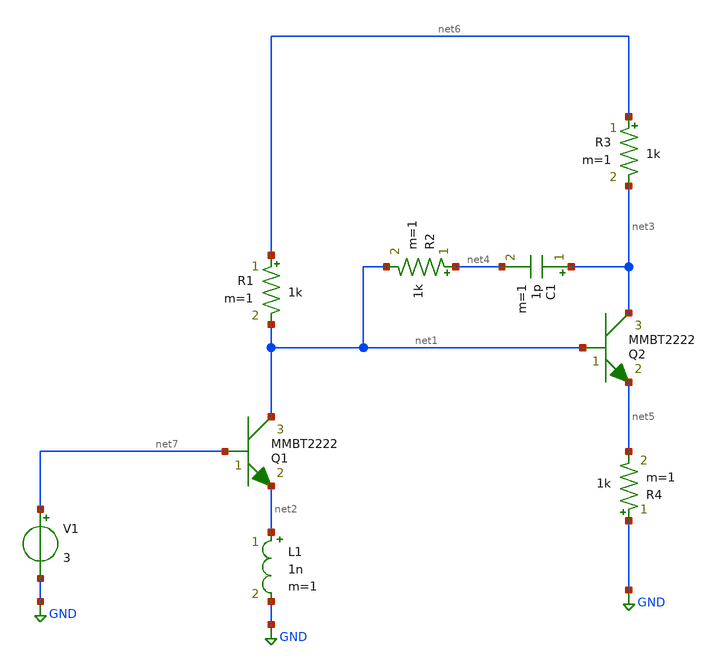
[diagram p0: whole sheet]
** sch_path: poweramp/poweramp.sch
**.subckt poweramp
Q2 net3 net1 net5 MMBT2222 area=1 m=1
Q1 net1 net7 net2 MMBT2222 area=1 m=1
R1 net6 net1 1k m=1
R2 net4 net1 1k m=1
C1 net3 net4 1p m=1
R3 net6 net3 1k m=1
L1 net2 GND 1n m=1
R4 GND net5 1k m=1
V1 net7 GND 3
**.ends
.GLOBAL GND
.end
